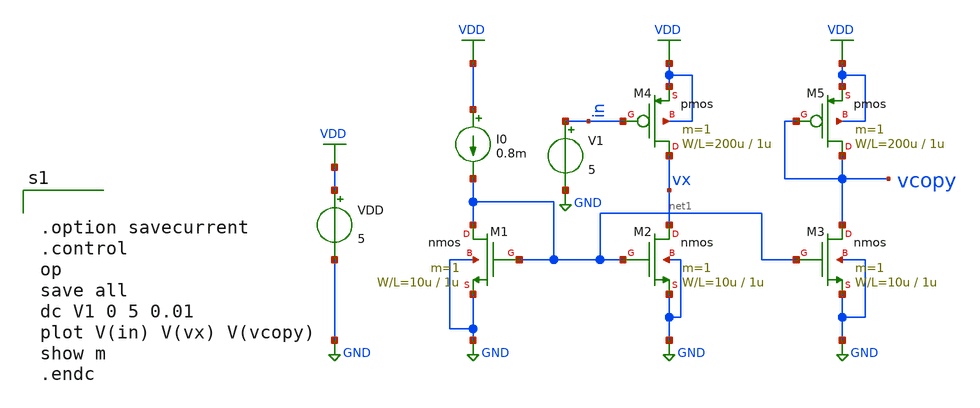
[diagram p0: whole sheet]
** sch_path: member_project/GroupWork/Team_masahiro/bias_replica.sch
**.subckt bias_replica
M1 net1 net1 GND GND nmos L=1u W=10u m=1
I0 VDD net1 0.8m
M2 vx net1 GND GND nmos L=1u W=10u m=1
VDD VDD GND 5
M3 vcopy net1 GND GND nmos L=1u W=10u m=1
M4 vx in VDD VDD pmos L=1u W=200u m=1
M5 vcopy vcopy VDD VDD pmos L=1u W=200u m=1
V1 in GND 5
**** begin user architecture code
 .include $::LIB/mos.lib
.include $::LIB/passive.lib
.include $::LIB/diode.lib


.option savecurrent
.control
op
save all
dc V1 0 5 0.01
plot V(in) V(vx) V(vcopy)
show m
.endc


**** end user architecture code
**.ends
.GLOBAL GND
.GLOBAL VDD
.end
